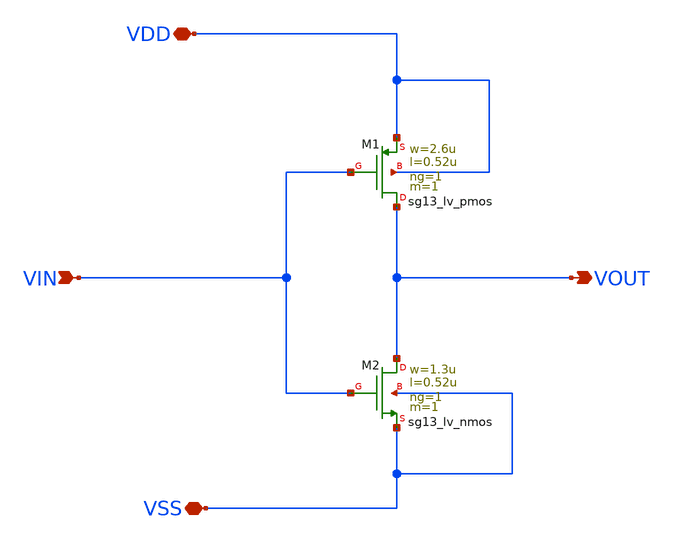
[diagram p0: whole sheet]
** sch_path: lab/Analog_Inverter/1_schematics/Analog_Inverter.sch
* (c) 2024 Hrishikesh, @HSB
**.subckt Analog_Inverter VIN VDD VSS VOUT
*.ipin VIN
*.iopin VDD
*.iopin VSS
*.opin VOUT
XM1 VOUT VIN VDD VDD sg13_lv_pmos w=2.6u l=0.52u ng=1 m=1 mm_ok=1
XM2 VOUT VIN VSS VSS sg13_lv_nmos w=1.3u l=0.52u ng=1 m=1 mm_ok=1
**.ends
.end
